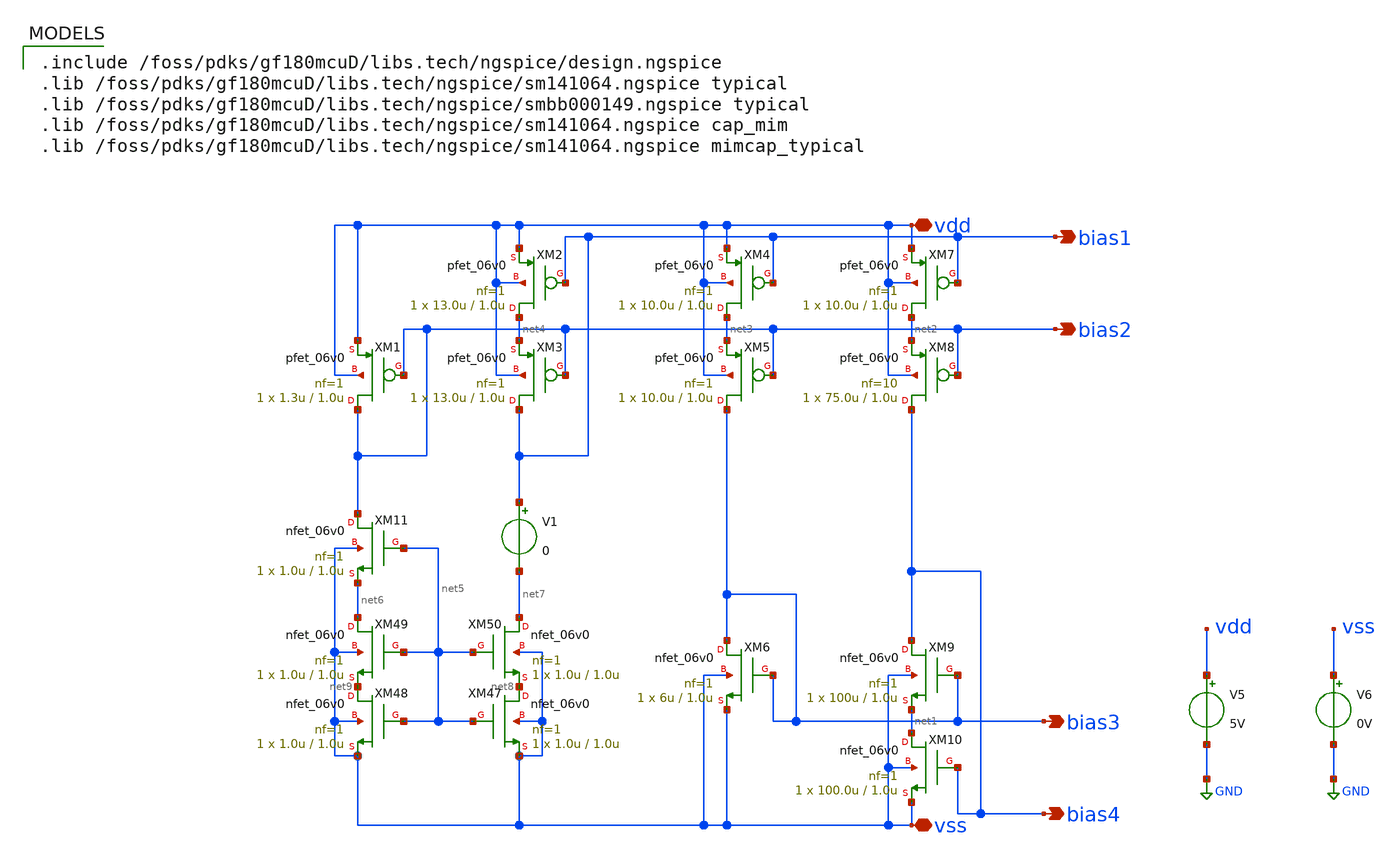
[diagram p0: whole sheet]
** sch_path: activities/opamp2AKAM/simulations_testbench/simulations_testbench/biasTestbench.sch
**.subckt biasTestbench bias1 bias2 bias3 bias4 vdd vss
*.opin bias1
*.opin bias2
*.opin bias3
*.opin bias4
*.iopin vdd
*.iopin vss
V5 vdd GND 5V
V6 vss GND 0V
XM4 net3 bias1 vdd vdd pfet_06v0 L=1.0u W=10.0u nf=1 ad='int((nf+1)/2) * W/nf * 0.18u' as='int((nf+2)/2) * W/nf * 0.18u'
+ pd='2*int((nf+1)/2) * (W/nf + 0.18u)' ps='2*int((nf+2)/2) * (W/nf + 0.18u)' nrd='0.18u / W' nrs='0.18u / W'
+ sa=0 sb=0 sd=0 m=1
XM5 bias3 bias2 net3 vdd pfet_06v0 L=1.0u W=10.0u nf=1 ad='int((nf+1)/2) * W/nf * 0.18u' as='int((nf+2)/2) * W/nf * 0.18u'
+ pd='2*int((nf+1)/2) * (W/nf + 0.18u)' ps='2*int((nf+2)/2) * (W/nf + 0.18u)' nrd='0.18u / W' nrs='0.18u / W'
+ sa=0 sb=0 sd=0 m=1
XM6 bias3 bias3 vss vss nfet_06v0 L=1.0u W=6u nf=1 ad='int((nf+1)/2) * W/nf * 0.18u' as='int((nf+2)/2) * W/nf * 0.18u'
+ pd='2*int((nf+1)/2) * (W/nf + 0.18u)' ps='2*int((nf+2)/2) * (W/nf + 0.18u)' nrd='0.18u / W' nrs='0.18u / W'
+ sa=0 sb=0 sd=0 m=1
XM7 net2 bias1 vdd vdd pfet_06v0 L=1.0u W=10.0u nf=1 ad='int((nf+1)/2) * W/nf * 0.18u' as='int((nf+2)/2) * W/nf * 0.18u'
+ pd='2*int((nf+1)/2) * (W/nf + 0.18u)' ps='2*int((nf+2)/2) * (W/nf + 0.18u)' nrd='0.18u / W' nrs='0.18u / W'
+ sa=0 sb=0 sd=0 m=1
XM8 bias4 bias2 net2 vdd pfet_06v0 L=1.0u W=75.0u nf=10 ad='int((nf+1)/2) * W/nf * 0.18u' as='int((nf+2)/2) * W/nf * 0.18u'
+ pd='2*int((nf+1)/2) * (W/nf + 0.18u)' ps='2*int((nf+2)/2) * (W/nf + 0.18u)' nrd='0.18u / W' nrs='0.18u / W'
+ sa=0 sb=0 sd=0 m=1
XM9 bias4 bias3 net1 vss nfet_06v0 L=1.0u W=100u nf=1 ad='int((nf+1)/2) * W/nf * 0.18u' as='int((nf+2)/2) * W/nf * 0.18u'
+ pd='2*int((nf+1)/2) * (W/nf + 0.18u)' ps='2*int((nf+2)/2) * (W/nf + 0.18u)' nrd='0.18u / W' nrs='0.18u / W'
+ sa=0 sb=0 sd=0 m=1
XM10 net1 bias4 vss vss nfet_06v0 L=1.0u W=100.0u nf=1 ad='int((nf+1)/2) * W/nf * 0.18u' as='int((nf+2)/2) * W/nf * 0.18u'
+ pd='2*int((nf+1)/2) * (W/nf + 0.18u)' ps='2*int((nf+2)/2) * (W/nf + 0.18u)' nrd='0.18u / W' nrs='0.18u / W'
+ sa=0 sb=0 sd=0 m=1
XM1 bias2 bias2 vdd vdd pfet_06v0 L=1.0u W=1.3u nf=1 ad='int((nf+1)/2) * W/nf * 0.18u' as='int((nf+2)/2) * W/nf * 0.18u'
+ pd='2*int((nf+1)/2) * (W/nf + 0.18u)' ps='2*int((nf+2)/2) * (W/nf + 0.18u)' nrd='0.18u / W' nrs='0.18u / W'
+ sa=0 sb=0 sd=0 m=1
XM2 net4 bias1 vdd vdd pfet_06v0 L=1.0u W=13.0u nf=1 ad='int((nf+1)/2) * W/nf * 0.18u' as='int((nf+2)/2) * W/nf * 0.18u'
+ pd='2*int((nf+1)/2) * (W/nf + 0.18u)' ps='2*int((nf+2)/2) * (W/nf + 0.18u)' nrd='0.18u / W' nrs='0.18u / W'
+ sa=0 sb=0 sd=0 m=1
XM3 bias1 bias2 net4 vdd pfet_06v0 L=1.0u W=13.0u nf=1 ad='int((nf+1)/2) * W/nf * 0.18u' as='int((nf+2)/2) * W/nf * 0.18u'
+ pd='2*int((nf+1)/2) * (W/nf + 0.18u)' ps='2*int((nf+2)/2) * (W/nf + 0.18u)' nrd='0.18u / W' nrs='0.18u / W'
+ sa=0 sb=0 sd=0 m=1
XM47 net8 net5 vss vss nfet_06v0 L=1.0u W=1.0u nf=1 ad='int((nf+1)/2) * W/nf * 0.18u' as='int((nf+2)/2) * W/nf * 0.18u'
+ pd='2*int((nf+1)/2) * (W/nf + 0.18u)' ps='2*int((nf+2)/2) * (W/nf + 0.18u)' nrd='0.18u / W' nrs='0.18u / W'
+ sa=0 sb=0 sd=0 m=1
XM48 net9 net5 vss vss nfet_06v0 L=1.0u W=1.0u nf=1 ad='int((nf+1)/2) * W/nf * 0.18u' as='int((nf+2)/2) * W/nf * 0.18u'
+ pd='2*int((nf+1)/2) * (W/nf + 0.18u)' ps='2*int((nf+2)/2) * (W/nf + 0.18u)' nrd='0.18u / W' nrs='0.18u / W'
+ sa=0 sb=0 sd=0 m=1
XM49 net6 net5 net9 vss nfet_06v0 L=1.0u W=1.0u nf=1 ad='int((nf+1)/2) * W/nf * 0.18u' as='int((nf+2)/2) * W/nf * 0.18u'
+ pd='2*int((nf+1)/2) * (W/nf + 0.18u)' ps='2*int((nf+2)/2) * (W/nf + 0.18u)' nrd='0.18u / W' nrs='0.18u / W'
+ sa=0 sb=0 sd=0 m=1
XM50 net7 net5 net8 vss nfet_06v0 L=1.0u W=1.0u nf=1 ad='int((nf+1)/2) * W/nf * 0.18u' as='int((nf+2)/2) * W/nf * 0.18u'
+ pd='2*int((nf+1)/2) * (W/nf + 0.18u)' ps='2*int((nf+2)/2) * (W/nf + 0.18u)' nrd='0.18u / W' nrs='0.18u / W'
+ sa=0 sb=0 sd=0 m=1
XM11 bias2 net5 net6 vss nfet_06v0 L=1.0u W=1.0u nf=1 ad='int((nf+1)/2) * W/nf * 0.18u' as='int((nf+2)/2) * W/nf * 0.18u'
+ pd='2*int((nf+1)/2) * (W/nf + 0.18u)' ps='2*int((nf+2)/2) * (W/nf + 0.18u)' nrd='0.18u / W' nrs='0.18u / W'
+ sa=0 sb=0 sd=0 m=1
V1 bias1 net7 0
**** begin user architecture code

.include /foss/pdks/gf180mcuD/libs.tech/ngspice/design.ngspice
.lib /foss/pdks/gf180mcuD/libs.tech/ngspice/sm141064.ngspice typical
.lib /foss/pdks/gf180mcuD/libs.tech/ngspice/smbb000149.ngspice typical
.lib /foss/pdks/gf180mcuD/libs.tech/ngspice/sm141064.ngspice cap_mim
.lib /foss/pdks/gf180mcuD/libs.tech/ngspice/sm141064.ngspice mimcap_typical



.tran 1ms 200ms
*.dc v3 -3.3 3.3 1m
.save all
.control
run
meas tran b1 find v(bias1) at=199ms
meas tran b2 find v(bias2) at=199ms
meas tran b3 find v(bias3) at=199ms
meas tran b4 find v(bias4) at=199ms
echo "$&b1 $&b2 $&b3 $&b4" >>
+ /foss/designs/sscs-2026-zotnetic/activities/opamp2AKAM/simulations_testbench/simulation_results/biasTestBench.txt
*let n = length(v(bias1))
*echo "$&v(bias1)[n-1] $&v(bias2)[n-1] $&v(bias3)[n-1] $&v(bias4)[n-1]" >>
*+ /foss/designs/sscs-2026-zotnetic/activities/opamp2AKAM/simulations_testbench/simulation_results/biasTestBench.txt
.endc
*.control
*  op
*  let b1 = v(bias1)
*  let b2 = v(bias2)
*  let b3 = v(bias3)
*  let b4 = v(bias4)
*  echo "$&b1 $&b2 $&b3 $&b4" >>
*+ /foss/designs/sscs-2026-zotnetic/activities/opamp2AKAM/simulations_testbench/simulation_results/biasTestBench.txt
*
*.endc


**** end user architecture code
**.ends
.GLOBAL GND
.end
